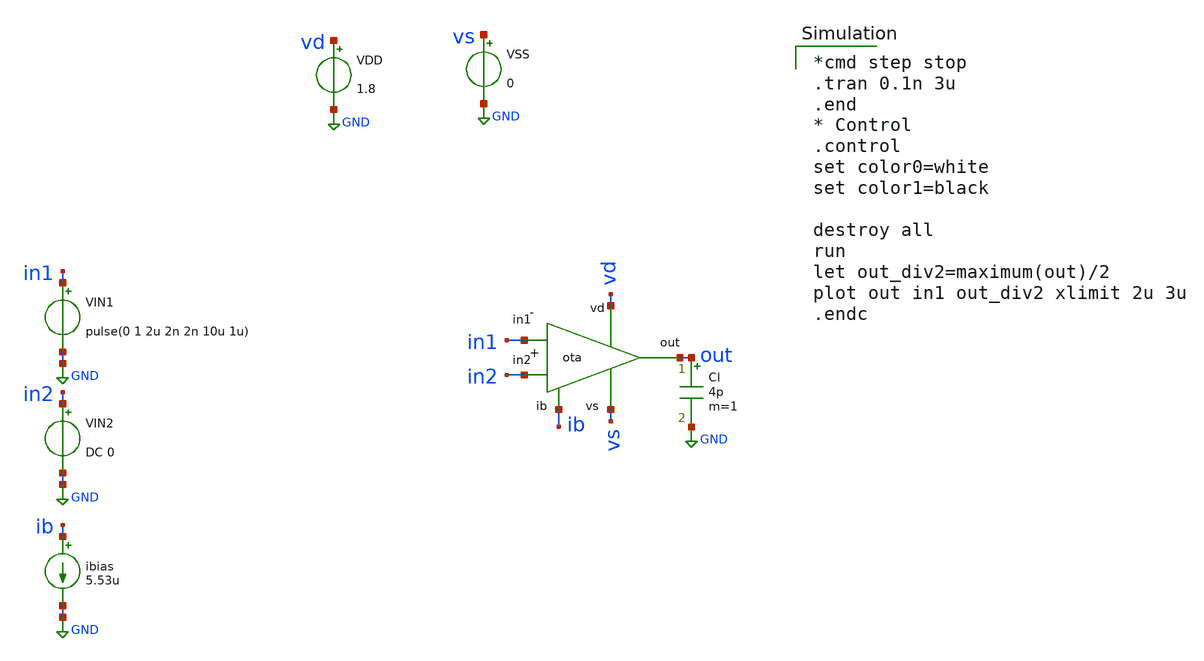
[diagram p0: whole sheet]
** sch_path: buffer/xschem/ota_tb-largesignal.sch
* Copyright 2020 Stefan Frederik Schippers
* Licensed under the Apache License, Version 2.0 (the "License");
* you may not use this file except in compliance with the License.
* You may obtain a copy of the License at
* https://www.apache.org/licenses/LICENSE-2.0
* Unless required by applicable law or agreed to in writing, software
* distributed under the License is distributed on an "AS IS" BASIS,
* WITHOUT WARRANTIES OR CONDITIONS OF ANY KIND, either express or implied.
* See the License for the specific language governing permissions and
* limitations under the License.
**.subckt ota_tb-largesignal
VIN2 in2 GND DC 0
VIN1 in1 GND pulse(0 1 2u 2n 2n 10u 1u)
ibias ib GND 5.53u
VDD vd GND 1.8
VSS vs GND 0
Cl out GND 4p m=1
X1 vd ib out in2 in1 vs ota
**** begin user architecture code

*cmd step stop
.tran 0.1n 3u
.end
* Control
.control
set color0=white
set color1=black

destroy all
run
let out_div2=maximum(out)/2
plot out in1 out_div2 xlimit 2u 3u
.endc

 .lib $::SKYWATER_MODELS/sky130.lib.spice tt
.include $::SKYWATER_STDCELLS/sky130_fd_sc_hd.spice

**** end user architecture code
**.ends

* expanding   symbol:  /home/hugodg/projects-sky130/temp-sensor/amp-op/xschem/ota.sym # of pins=6
** sym_path: amp-op/xschem/ota.sym
** sch_path: amp-op/xschem/ota.sch
.subckt ota vd ib out in2 in1 vs
*.iopin vd
*.iopin vs
*.iopin ib
*.ipin in1
*.ipin in2
*.opin out
XCC out d sky130_fd_pr__cap_mim_m3_1 W=21 L=21 MF=1 m=1
XM5 ib ib vd vd sky130_fd_pr__pfet_01v8 L=1 W=6 nf=1 ad='int((nf+1)/2) * W/nf * 0.29' as='int((nf+2)/2) * W/nf * 0.29'
+ pd='2*int((nf+1)/2) * (W/nf + 0.29)' ps='2*int((nf+2)/2) * (W/nf + 0.29)' nrd='0.29 / W' nrs='0.29 / W'
+ sa=0 sb=0 sd=0 mult=1 m=1
XM6 b ib vd vd sky130_fd_pr__pfet_01v8 L=1 W=6 nf=1 ad='int((nf+1)/2) * W/nf * 0.29' as='int((nf+2)/2) * W/nf * 0.29'
+ pd='2*int((nf+1)/2) * (W/nf + 0.29)' ps='2*int((nf+2)/2) * (W/nf + 0.29)' nrd='0.29 / W' nrs='0.29 / W'
+ sa=0 sb=0 sd=0 mult=1 m=1
XM8 out ib vd vd sky130_fd_pr__pfet_01v8 L=1 W=30 nf=4 ad='int((nf+1)/2) * W/nf * 0.29' as='int((nf+2)/2) * W/nf * 0.29'
+ pd='2*int((nf+1)/2) * (W/nf + 0.29)' ps='2*int((nf+2)/2) * (W/nf + 0.29)' nrd='0.29 / W' nrs='0.29 / W'
+ sa=0 sb=0 sd=0 mult=1 m=1
XM1 c in1 b b sky130_fd_pr__pfet_01v8 L=1 W=3 nf=1 ad='int((nf+1)/2) * W/nf * 0.29' as='int((nf+2)/2) * W/nf * 0.29'
+ pd='2*int((nf+1)/2) * (W/nf + 0.29)' ps='2*int((nf+2)/2) * (W/nf + 0.29)' nrd='0.29 / W' nrs='0.29 / W'
+ sa=0 sb=0 sd=0 mult=1 m=1
XM2 d in2 b b sky130_fd_pr__pfet_01v8 L=1 W=3 nf=1 ad='int((nf+1)/2) * W/nf * 0.29' as='int((nf+2)/2) * W/nf * 0.29'
+ pd='2*int((nf+1)/2) * (W/nf + 0.29)' ps='2*int((nf+2)/2) * (W/nf + 0.29)' nrd='0.29 / W' nrs='0.29 / W'
+ sa=0 sb=0 sd=0 mult=1 m=1
XM3 c c vs vs sky130_fd_pr__nfet_01v8 L=1 W=1 nf=1 ad='int((nf+1)/2) * W/nf * 0.29' as='int((nf+2)/2) * W/nf * 0.29'
+ pd='2*int((nf+1)/2) * (W/nf + 0.29)' ps='2*int((nf+2)/2) * (W/nf + 0.29)' nrd='0.29 / W' nrs='0.29 / W'
+ sa=0 sb=0 sd=0 mult=1 m=1
XM4 d c vs vs sky130_fd_pr__nfet_01v8 L=1 W=1 nf=1 ad='int((nf+1)/2) * W/nf * 0.29' as='int((nf+2)/2) * W/nf * 0.29'
+ pd='2*int((nf+1)/2) * (W/nf + 0.29)' ps='2*int((nf+2)/2) * (W/nf + 0.29)' nrd='0.29 / W' nrs='0.29 / W'
+ sa=0 sb=0 sd=0 mult=1 m=1
XM7 out d vs vs sky130_fd_pr__nfet_01v8 L=1 W=9 nf=2 ad='int((nf+1)/2) * W/nf * 0.29' as='int((nf+2)/2) * W/nf * 0.29'
+ pd='2*int((nf+1)/2) * (W/nf + 0.29)' ps='2*int((nf+2)/2) * (W/nf + 0.29)' nrd='0.29 / W' nrs='0.29 / W'
+ sa=0 sb=0 sd=0 mult=1 m=1
.ends

.GLOBAL GND
.end
